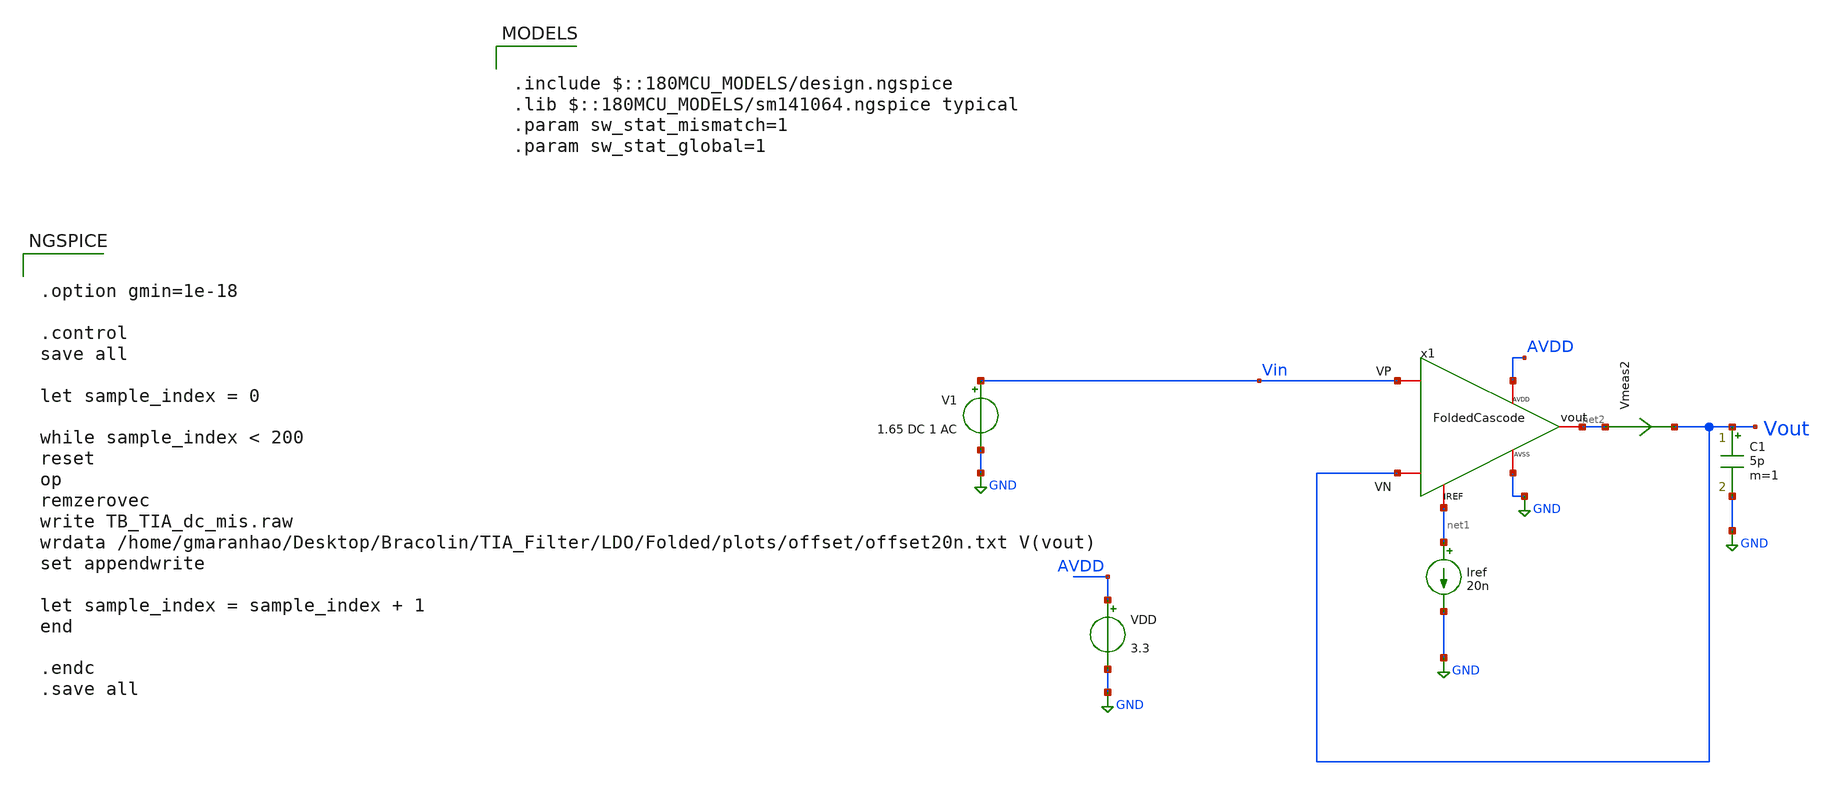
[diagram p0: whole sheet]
** sch_path: Voltage_Reference/LDO/Folded/TB_Folded_dc_mis.sch
**.subckt TB_Folded_dc_mis
VDD AVDD GND 3.3
Iref net1 GND 20n
Vmeas2 net2 Vout 0
.save i(vmeas2)
C1 Vout GND 5p m=1
x1 Vin Vout net2 net1 AVDD GND FoldedCascode
V1 Vin GND 1.65 DC 1 AC
**** begin user architecture code

.include $::180MCU_MODELS/design.ngspice
.lib $::180MCU_MODELS/sm141064.ngspice typical
.param sw_stat_mismatch=1
.param sw_stat_global=1



.option gmin=1e-18

.control
save all

let sample_index = 0

while sample_index < 200
reset
op
remzerovec
write TB_TIA_dc_mis.raw
wrdata /home/gmaranhao/Desktop/Bracolin/TIA_Filter/LDO/Folded/plots/offset/offset20n.txt V(vout)
set appendwrite

let sample_index = sample_index + 1
end

.endc
.save all


**** end user architecture code
**.ends
.GLOBAL GND
.end
